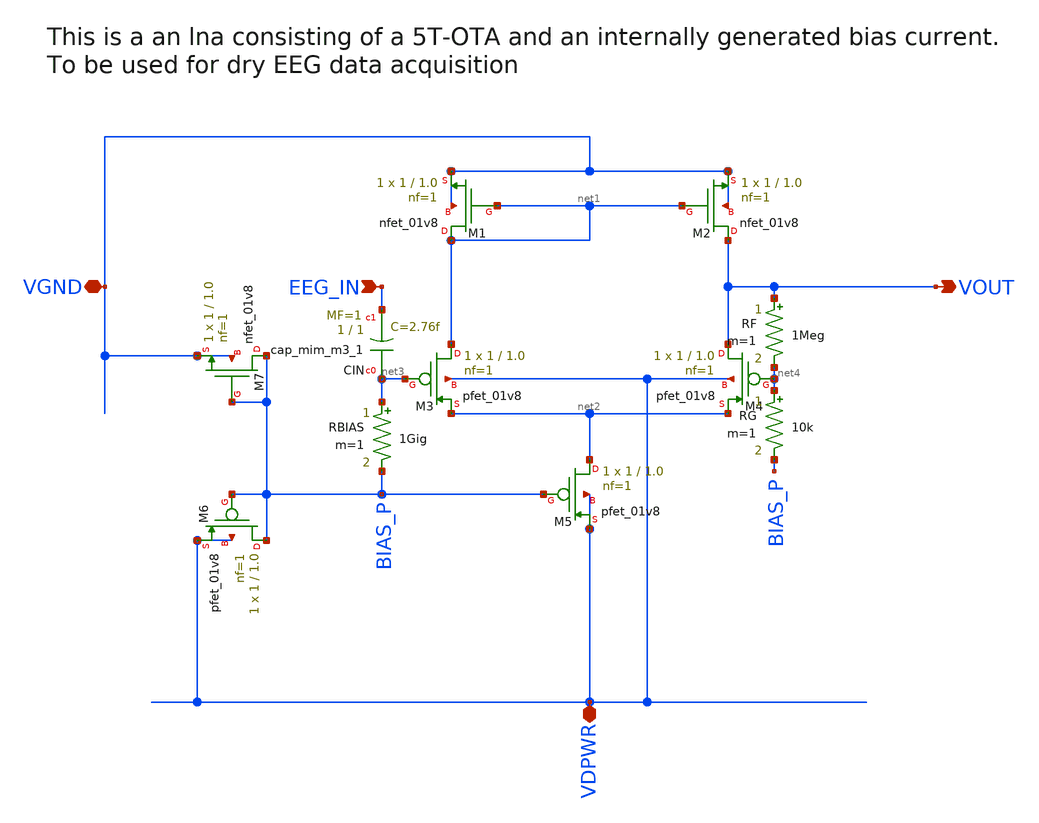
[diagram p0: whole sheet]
** sch_path: xschem/eeg_lna.sch
**.subckt eeg_lna VGND EEG_IN VDPWR VOUT
*.iopin VGND
*.ipin EEG_IN
*.iopin VDPWR
*.opin VOUT
MM1 net1 net1 VGND VGND sky130_fd_pr__nfet_01v8 L=1.0 W=1 nf=1 ad='int((1 + 1)/2) * 1 / 1 * 0.29' as='int((1 + 2)/2) * 1 / 1 * 0.29'
+ pd='2*int((1 + 1)/2) * (1 / 1 + 0.29)' ps='2*int((1 + 2)/2) * (1 / 1 + 0.29)' nrd='0.29 / 1 ' nrs='0.29 / 1 '
+ sa=0 sb=0 sd=0 mult=1 m=1
MM2 VOUT net1 VGND VGND sky130_fd_pr__nfet_01v8 L=1.0 W=1 nf=1 ad='int((1 + 1)/2) * 1 / 1 * 0.29' as='int((1 + 2)/2) * 1 / 1 * 0.29'
+ pd='2*int((1 + 1)/2) * (1 / 1 + 0.29)' ps='2*int((1 + 2)/2) * (1 / 1 + 0.29)' nrd='0.29 / 1 ' nrs='0.29 / 1 '
+ sa=0 sb=0 sd=0 mult=1 m=1
MM3 net1 net3 net2 VDPWR sky130_fd_pr__pfet_01v8 L=1.0 W=1 nf=1 ad='int((1 + 1)/2) * 1 / 1 * 0.29' as='int((1 + 2)/2) * 1 / 1 * 0.29'
+ pd='2*int((1 + 1)/2) * (1 / 1 + 0.29)' ps='2*int((1 + 2)/2) * (1 / 1 + 0.29)' nrd='0.29 / 1 ' nrs='0.29 / 1 '
+ sa=0 sb=0 sd=0 mult=1 m=1
MM4 VOUT net4 net2 VDPWR sky130_fd_pr__pfet_01v8 L=1.0 W=1 nf=1 ad='int((1 + 1)/2) * 1 / 1 * 0.29' as='int((1 + 2)/2) * 1 / 1 * 0.29'
+ pd='2*int((1 + 1)/2) * (1 / 1 + 0.29)' ps='2*int((1 + 2)/2) * (1 / 1 + 0.29)' nrd='0.29 / 1 ' nrs='0.29 / 1 '
+ sa=0 sb=0 sd=0 mult=1 m=1
MM5 net2 BIAS_P VDPWR VDPWR sky130_fd_pr__pfet_01v8 L=1.0 W=1 nf=1 ad='int((1 + 1)/2) * 1 / 1 * 0.29'
+ as='int((1 + 2)/2) * 1 / 1 * 0.29' pd='2*int((1 + 1)/2) * (1 / 1 + 0.29)' ps='2*int((1 + 2)/2) * (1 / 1 + 0.29)'
+ nrd='0.29 / 1 ' nrs='0.29 / 1 ' sa=0 sb=0 sd=0 mult=1 m=1
MM6 BIAS_P BIAS_P VDPWR VDPWR sky130_fd_pr__pfet_01v8 L=1.0 W=1 nf=1 ad='int((1 + 1)/2) * 1 / 1 * 0.29'
+ as='int((1 + 2)/2) * 1 / 1 * 0.29' pd='2*int((1 + 1)/2) * (1 / 1 + 0.29)' ps='2*int((1 + 2)/2) * (1 / 1 + 0.29)'
+ nrd='0.29 / 1 ' nrs='0.29 / 1 ' sa=0 sb=0 sd=0 mult=1 m=1
MM7 BIAS_P BIAS_P VGND VGND sky130_fd_pr__nfet_01v8 L=1.0 W=1 nf=1 ad='int((1 + 1)/2) * 1 / 1 * 0.29'
+ as='int((1 + 2)/2) * 1 / 1 * 0.29' pd='2*int((1 + 1)/2) * (1 / 1 + 0.29)' ps='2*int((1 + 2)/2) * (1 / 1 + 0.29)'
+ nrd='0.29 / 1 ' nrs='0.29 / 1 ' sa=0 sb=0 sd=0 mult=1 m=1
XCIN net3 EEG_IN sky130_fd_pr__cap_mim_m3_1 W=1 L=1 MF=1 m=1
RBIAS net3 BIAS_P 1Gig m=1
RF VOUT net4 1Meg m=1
RG net4 BIAS_P 10k m=1
**.ends
.end
